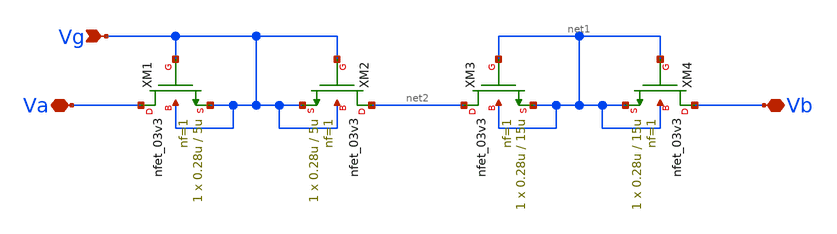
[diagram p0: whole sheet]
** sch_path: designs/libs/core_ina/ina_pseudores/ina_pseudores.sch
**.subckt ina_pseudores Vg Va Vb
*.ipin Vg
*.iopin Va
*.iopin Vb
XM1 Va Vg Vg Vg nfet_03v3 L=5u W=0.28u nf=1 ad='int((nf+1)/2) * W/nf * 0.18u' as='int((nf+2)/2) * W/nf * 0.18u'
+ pd='2*int((nf+1)/2) * (W/nf + 0.18u)' ps='2*int((nf+2)/2) * (W/nf + 0.18u)' nrd='0.18u / W' nrs='0.18u / W'
+ sa=0 sb=0 sd=0 m=1
XM2 net2 Vg Vg Vg nfet_03v3 L=5u W=0.28u nf=1 ad='int((nf+1)/2) * W/nf * 0.18u' as='int((nf+2)/2) * W/nf * 0.18u'
+ pd='2*int((nf+1)/2) * (W/nf + 0.18u)' ps='2*int((nf+2)/2) * (W/nf + 0.18u)' nrd='0.18u / W' nrs='0.18u / W'
+ sa=0 sb=0 sd=0 m=1
XM3 net2 net1 net1 net1 nfet_03v3 L=15u W=0.28u nf=1 ad='int((nf+1)/2) * W/nf * 0.18u' as='int((nf+2)/2) * W/nf * 0.18u'
+ pd='2*int((nf+1)/2) * (W/nf + 0.18u)' ps='2*int((nf+2)/2) * (W/nf + 0.18u)' nrd='0.18u / W' nrs='0.18u / W'
+ sa=0 sb=0 sd=0 m=1
XM4 Vb net1 net1 net1 nfet_03v3 L=15u W=0.28u nf=1 ad='int((nf+1)/2) * W/nf * 0.18u' as='int((nf+2)/2) * W/nf * 0.18u'
+ pd='2*int((nf+1)/2) * (W/nf + 0.18u)' ps='2*int((nf+2)/2) * (W/nf + 0.18u)' nrd='0.18u / W' nrs='0.18u / W'
+ sa=0 sb=0 sd=0 m=1
**.ends
.end
